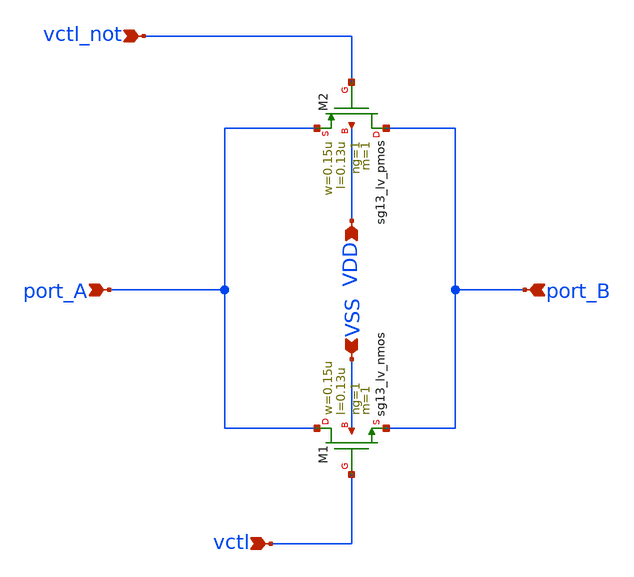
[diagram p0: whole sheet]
** sch_path: analog-db/circuits/sw_001_transmission_gate_pair/pdk/ihp-sg13g2/schematic/transmission_gate_pair.sch
* Copyright 2026 MacAnalog Research Group
**.subckt transmission_gate_pair port_A port_B vctl VSS VDD vctl_not
*.ipin port_A
*.ipin port_B
*.ipin vctl
*.ipin VSS
*.ipin VDD
*.ipin vctl_not
XM1 port_A vctl port_B VSS sg13_lv_nmos w=0.15u l=0.13u ng=1 m=1 mm_ok=1
XM2 port_B vctl_not port_A VDD sg13_lv_pmos w=0.15u l=0.13u ng=1 m=1 mm_ok=1
**.ends
.end
